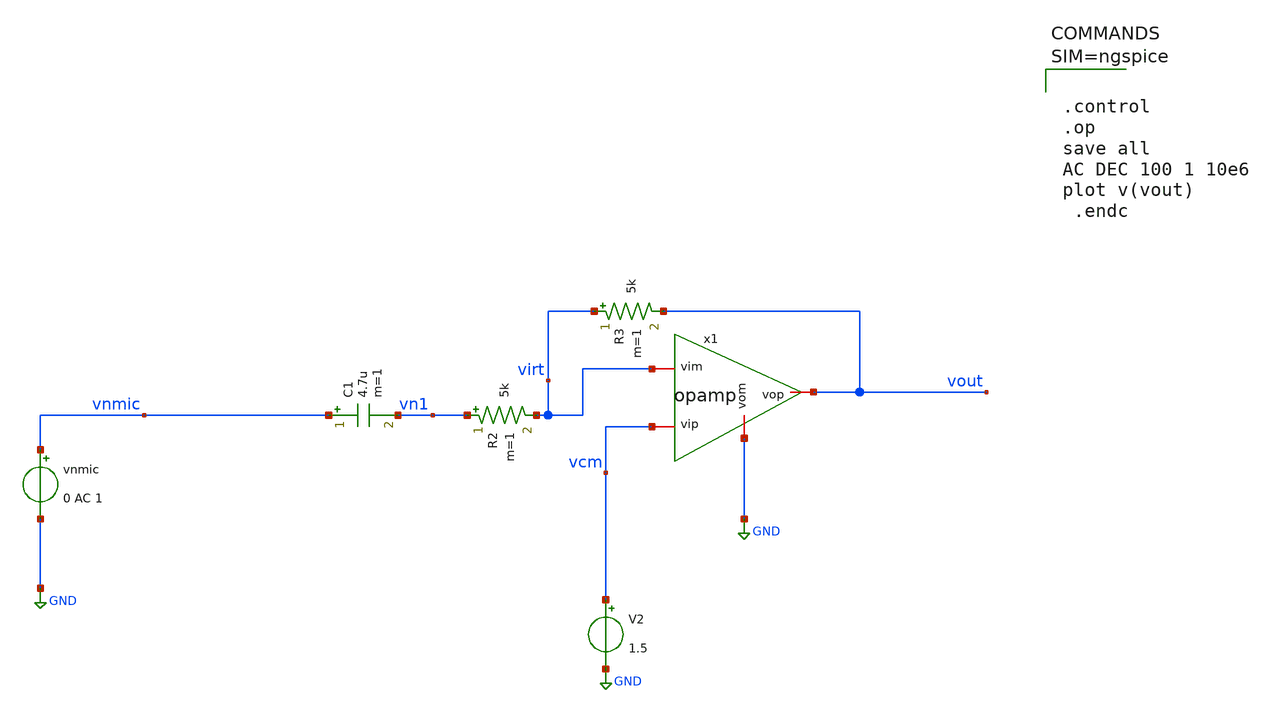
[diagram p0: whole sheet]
** sch_path: xschem/mictest_opamp.sch
**.subckt mictest_opamp
vnmic vnmic GND 0 AC 1
C1 vnmic vn1 4.7u m=1
R2 vn1 virt 5k m=1
R3 virt vout 5k m=1
V2 vcm GND 1.5
x1 vout vcm virt GND opamp
**** begin user architecture code



.control
.op
save all
AC DEC 100 1 10e6
plot v(vout)
 .endc



**** end user architecture code
**.ends

* expanding   symbol:  opamp.sym # of pins=4
** sym_path: xschem/opamp.sym
** sch_path: xschem/opamp.sch
.subckt opamp vop vip vim vom
*.iopin vop
*.iopin vom
*.iopin vim
*.iopin vip
E1 vop vom vip vim 1000
.ends

.GLOBAL GND
.end
